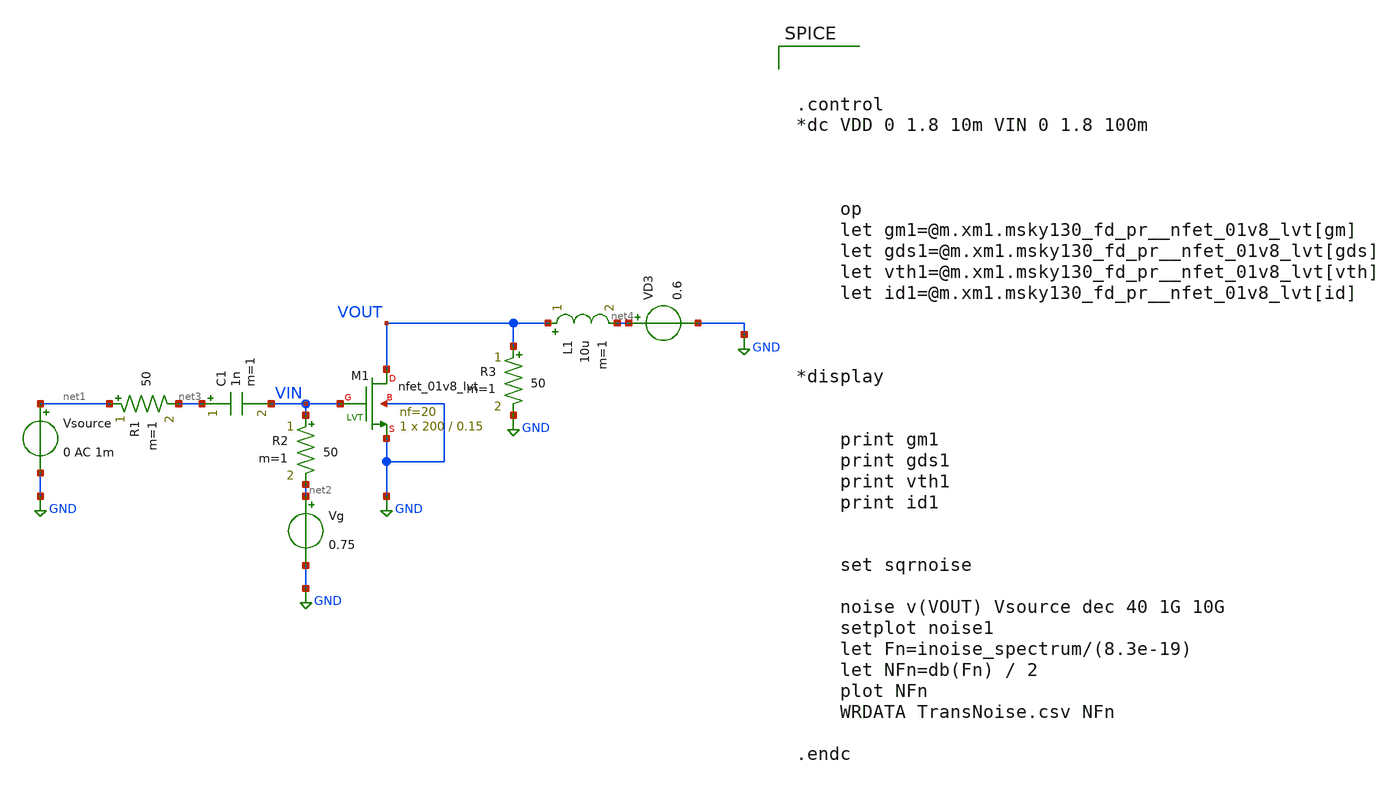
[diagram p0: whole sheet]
** sch_path: xschem/TransistorNoise.sch
**.subckt TransistorNoise
Vsource net1 GND 0 AC 1m
VD3 net4 GND 0.6
XM1 VOUT VIN GND GND sky130_fd_pr__nfet_01v8_lvt L=0.15 W=200 nf=20 ad='int((nf+1)/2) * W/nf * 0.29'
+ as='int((nf+2)/2) * W/nf * 0.29' pd='2*int((nf+1)/2) * (W/nf + 0.29)' ps='2*int((nf+2)/2) * (W/nf + 0.29)'
+ nrd='0.29 / W' nrs='0.29 / W' sa=0 sb=0 sd=0 mult=1 m=1
R1 net1 net3 50 m=1
R2 VIN net2 50 m=1
Vg net2 GND 0.75
C1 net3 VIN 1n m=1
L1 VOUT net4 10u m=1
R3 VOUT GND 50 m=1
**** begin user architecture code

.lib $::SKYWATER_MODELS/sky130.lib.spice tt




.control
*dc VDD 0 1.8 10m VIN 0 1.8 100m



	op
	let gm1=@m.xm1.msky130_fd_pr__nfet_01v8_lvt[gm]
	let gds1=@m.xm1.msky130_fd_pr__nfet_01v8_lvt[gds]
	let vth1=@m.xm1.msky130_fd_pr__nfet_01v8_lvt[vth]
	let id1=@m.xm1.msky130_fd_pr__nfet_01v8_lvt[id]



*display


	print gm1
	print gds1
	print vth1
	print id1


	set sqrnoise

	noise v(VOUT) Vsource dec 40 1G 10G
	setplot noise1
	let Fn=inoise_spectrum/(8.3e-19)
	let NFn=db(Fn) / 2
	plot NFn
	WRDATA TransNoise.csv NFn

.endc


**** end user architecture code
**.ends
.GLOBAL GND
.end
